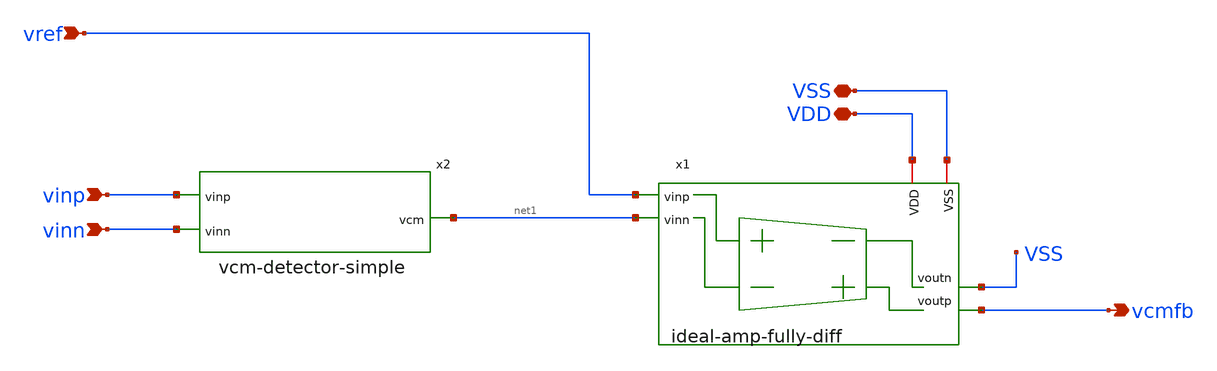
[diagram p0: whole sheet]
** sch_path: analog-db/drawings/shared/ideal/cmfb-output-ideal-amp-inv.sch
* Copyright 2026 MacAnalog Research Group
**.subckt cmfb-output-ideal-amp-inv VSS VDD vinp vinn vcmfb vref
*.iopin VSS
*.iopin VDD
*.ipin vinp
*.ipin vinn
*.opin vcmfb
*.ipin vref
x1 vref net1 VSS vcmfb VSS VDD ideal-amp-fully-diff
x2 net1 vinp vinn vcm-detector-simple
**.ends
.end
